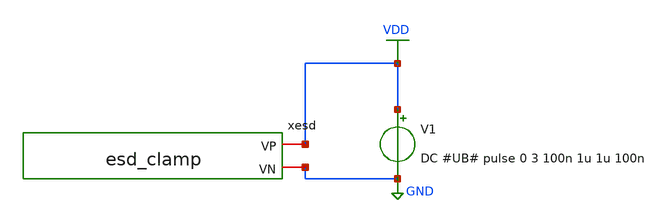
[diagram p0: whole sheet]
** sch_path: xschem/test/test_esd_mc.sch
**.subckt test_esd_mc
xesd VDD GND esd_clamp
V1 VDD GND DC #UB# pulse 0 3 100n 1u 1u 100n
**** begin user architecture code


.options savecurrents
.option warn=1
.control
set wr_vecnames
set wr_singlescale
set hcopydevtype=svg
set ITL1=10000

set model="#model#"
let mc_runs=100
let mc_runNo = 1

dowhile mc_runNo <= mc_runs
   destroy all
	let min_temp=0
	let var_temp = min_temp
	let max_temp=100
	let temp_step=10
	dowhile var_temp <= max_temp
		option temp=$&var_temp
		tran 5n 5u
		wrdata 'result_tran_tran_{$&var_temp}deg_{$&mc_runNo}.csv' i(v1) v(vdd) v(xesd.VGM1)
		run
		reset
		op
		wrdata 'result_op_op_{$&var_temp}deg_{$&mc_runNo}.csv' i(v1) v(vdd) v(xesd.VGM1)
		run
		reset
		let var_temp = var_temp + temp_step
	end
	let  mc_runNo = mc_runNo +1
	reset
end

.endc




* .include ../../tia.spice
* .include ../../filter_diff.spice
* .include ../../cmm_sense3.spice

* .include esd_clamp.spice
.include ../../../esd_clamp.spice



.lib $::SKYWATER_MODELS/sky130.lib.spice #model#
* .lib $::SKYWATER_MODELS/sky130.lib.spice.tt.red tt
* .lib /home/simon/share/pdk/sky130A/libs.tech/ngspice/sky130.lib.spice.tt.red tt

**** end user architecture code
**.ends

* expanding   symbol:  /home/simon/code/asic/analog/esd/esd_clamp.sym # of pins=2
** sym_path: xschem/esd/esd_clamp.sym
** sch_path: xschem/esd/esd_clamp.sch
.subckt esd_clamp VP VN
*.iopin VP
*.iopin VN
XD1 net1 VGM1 sky130_fd_pr__diode_pw2nd_05v5 area=10e12 pj=4e6
XM3 VGM5 VN VP VP sky130_fd_pr__pfet_01v8 L=1 W=2 nf=1 ad='int((nf+1)/2) * W/nf * 0.29' as='int((nf+2)/2) * W/nf * 0.29'
+ pd='2*int((nf+1)/2) * (W/nf + 0.29)' ps='2*int((nf+2)/2) * (W/nf + 0.29)' nrd='0.29 / W' nrs='0.29 / W'
+ sa=0 sb=0 sd=0 mult=1 m=1
XM4 VGM1 VGM5 VP VP sky130_fd_pr__pfet_01v8 L=0.3 W=2 nf=1 ad='int((nf+1)/2) * W/nf * 0.29' as='int((nf+2)/2) * W/nf * 0.29'
+ pd='2*int((nf+1)/2) * (W/nf + 0.29)' ps='2*int((nf+2)/2) * (W/nf + 0.29)' nrd='0.29 / W' nrs='0.29 / W'
+ sa=0 sb=0 sd=0 mult=10 m=10
XM5 VGM1 VGM5 VN VN sky130_fd_pr__nfet_01v8_lvt L=1 W=2 nf=1 ad='int((nf+1)/2) * W/nf * 0.29' as='int((nf+2)/2) * W/nf * 0.29'
+ pd='2*int((nf+1)/2) * (W/nf + 0.29)' ps='2*int((nf+2)/2) * (W/nf + 0.29)' nrd='0.29 / W' nrs='0.29 / W'
+ sa=0 sb=0 sd=0 mult=1 m=1
XD2 VP net1 sky130_fd_pr__diode_pw2nd_05v5 area=10e12 pj=4e6
XM1 VP VGM1 VN VN sky130_fd_pr__nfet_01v8 L=0.3 W=2 nf=1 ad='int((nf+1)/2) * W/nf * 0.29' as='int((nf+2)/2) * W/nf * 0.29'
+ pd='2*int((nf+1)/2) * (W/nf + 0.29)' ps='2*int((nf+2)/2) * (W/nf + 0.29)' nrd='0.29 / W' nrs='0.29 / W'
+ sa=0 sb=0 sd=0 mult=1000 m=1000
XM6 net1 VP VN VN sky130_fd_pr__nfet_01v8 L=1 W=1 nf=1 ad='int((nf+1)/2) * W/nf * 0.29' as='int((nf+2)/2) * W/nf * 0.29'
+ pd='2*int((nf+1)/2) * (W/nf + 0.29)' ps='2*int((nf+2)/2) * (W/nf + 0.29)' nrd='0.29 / W' nrs='0.29 / W'
+ sa=0 sb=0 sd=0 mult=1 m=1
XM2 VGM5 VGM1 VN VN sky130_fd_pr__nfet_01v8 L=0.3 W=2 nf=1 ad='int((nf+1)/2) * W/nf * 0.29' as='int((nf+2)/2) * W/nf * 0.29'
+ pd='2*int((nf+1)/2) * (W/nf + 0.29)' ps='2*int((nf+2)/2) * (W/nf + 0.29)' nrd='0.29 / W' nrs='0.29 / W'
+ sa=0 sb=0 sd=0 mult=10 m=10
.ends

.GLOBAL VDD
.GLOBAL GND
.end
